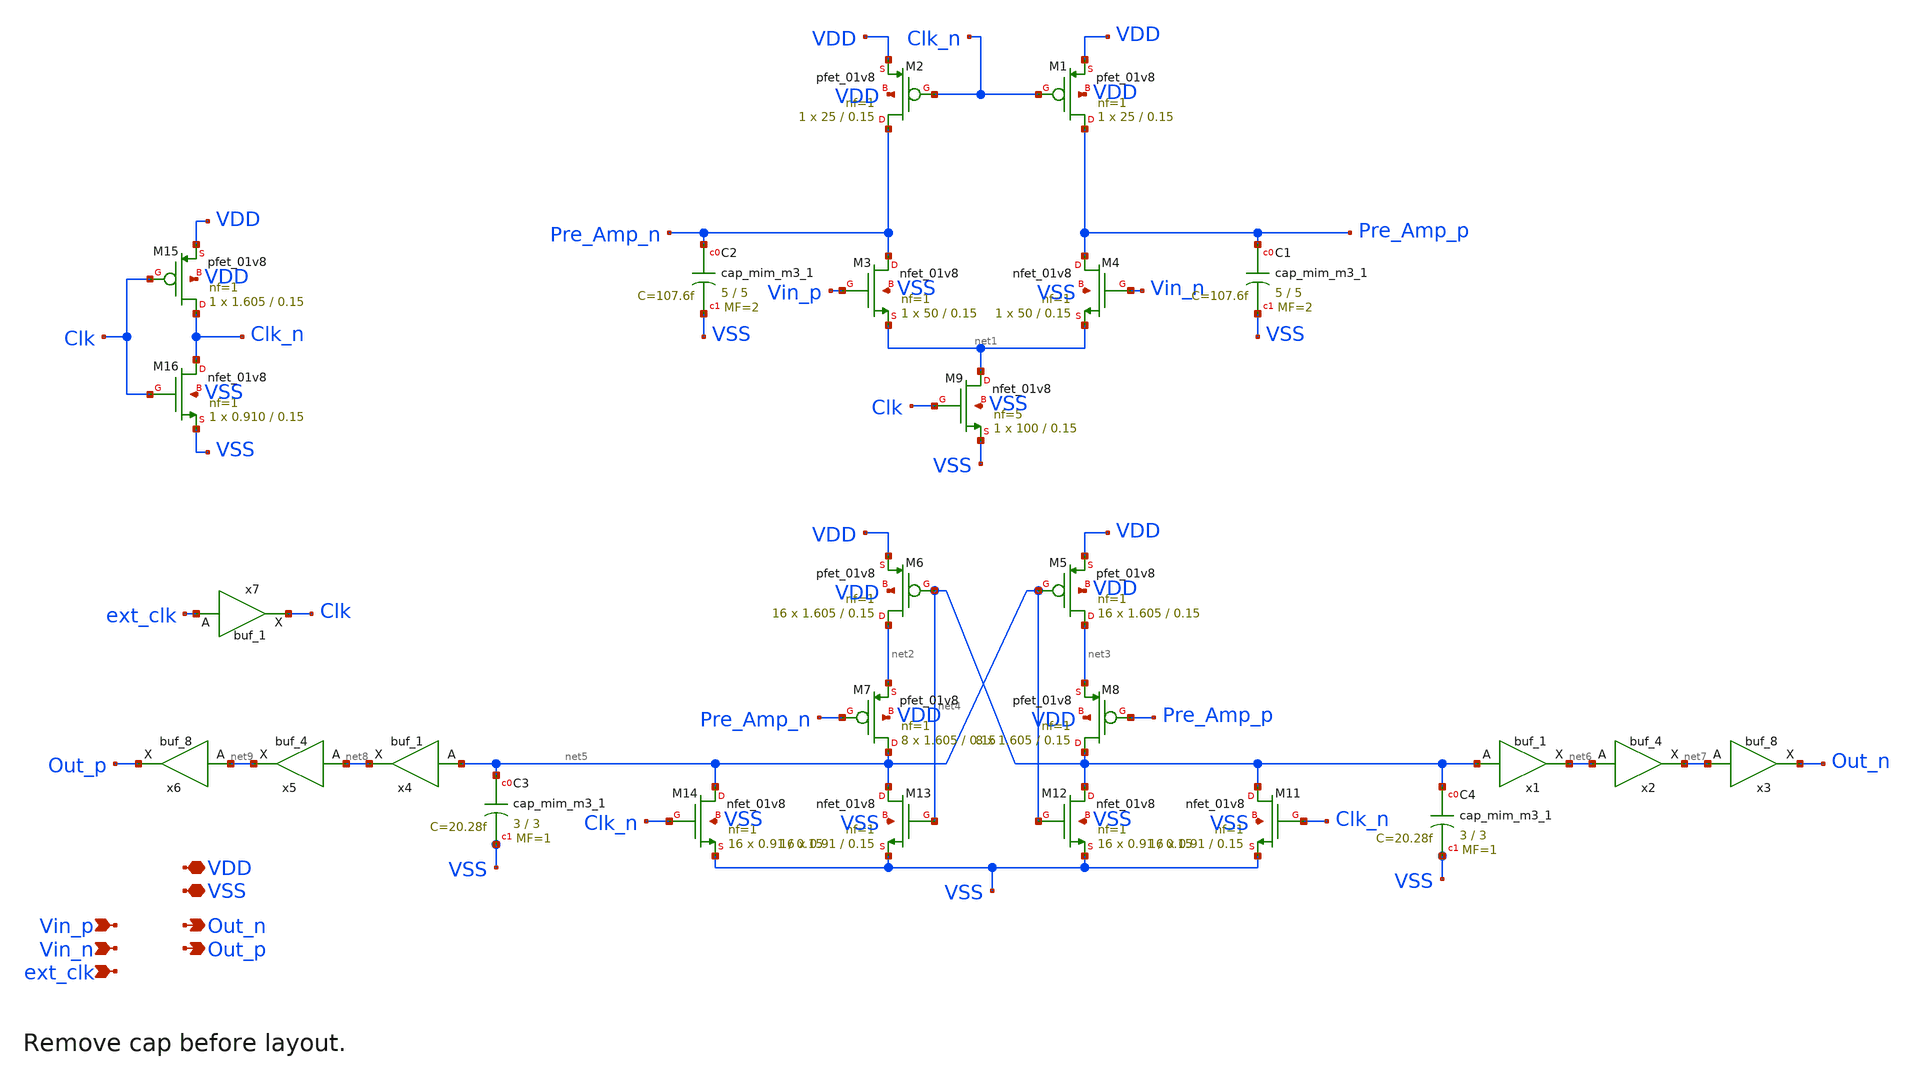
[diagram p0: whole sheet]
** sch_path: xschem/src/comparator/comparator.sch
**.subckt comparator VDD VSS Vin_p Out_n Vin_n Out_p ext_clk
*.iopin VDD
*.iopin VSS
*.ipin Vin_p
*.opin Out_n
*.ipin Vin_n
*.opin Out_p
*.ipin ext_clk
XM1 Pre_Amp_p Clk_n VDD VDD sky130_fd_pr__pfet_01v8 L=0.15 W=25 nf=1 ad='int((nf+1)/2) * W/nf * 0.29'
+ as='int((nf+2)/2) * W/nf * 0.29' pd='2*int((nf+1)/2) * (W/nf + 0.29)' ps='2*int((nf+2)/2) * (W/nf + 0.29)'
+ nrd='0.29 / W' nrs='0.29 / W' sa=0 sb=0 sd=0 mult=1 m=1
XM2 Pre_Amp_n Clk_n VDD VDD sky130_fd_pr__pfet_01v8 L=0.15 W=25 nf=1 ad='int((nf+1)/2) * W/nf * 0.29'
+ as='int((nf+2)/2) * W/nf * 0.29' pd='2*int((nf+1)/2) * (W/nf + 0.29)' ps='2*int((nf+2)/2) * (W/nf + 0.29)'
+ nrd='0.29 / W' nrs='0.29 / W' sa=0 sb=0 sd=0 mult=1 m=1
XM3 Pre_Amp_n Vin_p net1 VSS sky130_fd_pr__nfet_01v8 L=0.15 W=50 nf=1 ad='int((nf+1)/2) * W/nf * 0.29'
+ as='int((nf+2)/2) * W/nf * 0.29' pd='2*int((nf+1)/2) * (W/nf + 0.29)' ps='2*int((nf+2)/2) * (W/nf + 0.29)'
+ nrd='0.29 / W' nrs='0.29 / W' sa=0 sb=0 sd=0 mult=1 m=1
XM4 Pre_Amp_p Vin_n net1 VSS sky130_fd_pr__nfet_01v8 L=0.15 W=50 nf=1 ad='int((nf+1)/2) * W/nf * 0.29'
+ as='int((nf+2)/2) * W/nf * 0.29' pd='2*int((nf+1)/2) * (W/nf + 0.29)' ps='2*int((nf+2)/2) * (W/nf + 0.29)'
+ nrd='0.29 / W' nrs='0.29 / W' sa=0 sb=0 sd=0 mult=1 m=1
XM5 net3 net5 VDD VDD sky130_fd_pr__pfet_01v8 L=0.15 W=1.605 nf=1 ad='int((nf+1)/2) * W/nf * 0.29' as='int((nf+2)/2) * W/nf * 0.29'
+ pd='2*int((nf+1)/2) * (W/nf + 0.29)' ps='2*int((nf+2)/2) * (W/nf + 0.29)' nrd='0.29 / W' nrs='0.29 / W'
+ sa=0 sb=0 sd=0 mult=16 m=16
XM6 net2 net4 VDD VDD sky130_fd_pr__pfet_01v8 L=0.15 W=1.605 nf=1 ad='int((nf+1)/2) * W/nf * 0.29' as='int((nf+2)/2) * W/nf * 0.29'
+ pd='2*int((nf+1)/2) * (W/nf + 0.29)' ps='2*int((nf+2)/2) * (W/nf + 0.29)' nrd='0.29 / W' nrs='0.29 / W'
+ sa=0 sb=0 sd=0 mult=16 m=16
XM9 net1 Clk VSS VSS sky130_fd_pr__nfet_01v8 L=0.15 W=100 nf=5 ad='int((nf+1)/2) * W/nf * 0.29' as='int((nf+2)/2) * W/nf * 0.29'
+ pd='2*int((nf+1)/2) * (W/nf + 0.29)' ps='2*int((nf+2)/2) * (W/nf + 0.29)' nrd='0.29 / W' nrs='0.29 / W'
+ sa=0 sb=0 sd=0 mult=1 m=1
XM11 net4 Clk_n VSS VSS sky130_fd_pr__nfet_01v8 L=0.15 W=0.91 nf=1 ad='int((nf+1)/2) * W/nf * 0.29' as='int((nf+2)/2) * W/nf * 0.29'
+ pd='2*int((nf+1)/2) * (W/nf + 0.29)' ps='2*int((nf+2)/2) * (W/nf + 0.29)' nrd='0.29 / W' nrs='0.29 / W'
+ sa=0 sb=0 sd=0 mult=16 m=16
XM12 net4 net5 VSS VSS sky130_fd_pr__nfet_01v8 L=0.15 W=0.91 nf=1 ad='int((nf+1)/2) * W/nf * 0.29' as='int((nf+2)/2) * W/nf * 0.29'
+ pd='2*int((nf+1)/2) * (W/nf + 0.29)' ps='2*int((nf+2)/2) * (W/nf + 0.29)' nrd='0.29 / W' nrs='0.29 / W'
+ sa=0 sb=0 sd=0 mult=16 m=16
XM13 net5 net4 VSS VSS sky130_fd_pr__nfet_01v8 L=0.15 W=0.91 nf=1 ad='int((nf+1)/2) * W/nf * 0.29' as='int((nf+2)/2) * W/nf * 0.29'
+ pd='2*int((nf+1)/2) * (W/nf + 0.29)' ps='2*int((nf+2)/2) * (W/nf + 0.29)' nrd='0.29 / W' nrs='0.29 / W'
+ sa=0 sb=0 sd=0 mult=16 m=16
XM14 net5 Clk_n VSS VSS sky130_fd_pr__nfet_01v8 L=0.15 W=0.91 nf=1 ad='int((nf+1)/2) * W/nf * 0.29' as='int((nf+2)/2) * W/nf * 0.29'
+ pd='2*int((nf+1)/2) * (W/nf + 0.29)' ps='2*int((nf+2)/2) * (W/nf + 0.29)' nrd='0.29 / W' nrs='0.29 / W'
+ sa=0 sb=0 sd=0 mult=16 m=16
XM15 Clk_n Clk VDD VDD sky130_fd_pr__pfet_01v8 L=0.15 W=1.605 nf=1 ad='int((nf+1)/2) * W/nf * 0.29' as='int((nf+2)/2) * W/nf * 0.29'
+ pd='2*int((nf+1)/2) * (W/nf + 0.29)' ps='2*int((nf+2)/2) * (W/nf + 0.29)' nrd='0.29 / W' nrs='0.29 / W'
+ sa=0 sb=0 sd=0 mult=1 m=1
XM16 Clk_n Clk VSS VSS sky130_fd_pr__nfet_01v8 L=0.15 W=0.910 nf=1 ad='int((nf+1)/2) * W/nf * 0.29' as='int((nf+2)/2) * W/nf * 0.29'
+ pd='2*int((nf+1)/2) * (W/nf + 0.29)' ps='2*int((nf+2)/2) * (W/nf + 0.29)' nrd='0.29 / W' nrs='0.29 / W'
+ sa=0 sb=0 sd=0 mult=1 m=1
XM7 net5 Pre_Amp_n net2 VDD sky130_fd_pr__pfet_01v8 L=0.15 W=1.605 nf=1 ad='int((nf+1)/2) * W/nf * 0.29'
+ as='int((nf+2)/2) * W/nf * 0.29' pd='2*int((nf+1)/2) * (W/nf + 0.29)' ps='2*int((nf+2)/2) * (W/nf + 0.29)'
+ nrd='0.29 / W' nrs='0.29 / W' sa=0 sb=0 sd=0 mult=8 m=8
XM8 net4 Pre_Amp_p net3 VDD sky130_fd_pr__pfet_01v8 L=0.15 W=1.605 nf=1 ad='int((nf+1)/2) * W/nf * 0.29'
+ as='int((nf+2)/2) * W/nf * 0.29' pd='2*int((nf+1)/2) * (W/nf + 0.29)' ps='2*int((nf+2)/2) * (W/nf + 0.29)'
+ nrd='0.29 / W' nrs='0.29 / W' sa=0 sb=0 sd=0 mult=8 m=8
XC1 Pre_Amp_p VSS sky130_fd_pr__cap_mim_m3_1 W=5 L=5 MF=2 m=2
XC2 Pre_Amp_n VSS sky130_fd_pr__cap_mim_m3_1 W=5 L=5 MF=2 m=2
x1 net4 VSS VSS VDD VDD net6 sky130_fd_sc_hd__buf_1
x2 net6 VSS VSS VDD VDD net7 sky130_fd_sc_hd__buf_4
x3 net7 VSS VSS VDD VDD Out_n sky130_fd_sc_hd__buf_8
x4 net5 VSS VSS VDD VDD net8 sky130_fd_sc_hd__buf_1
x5 net8 VSS VSS VDD VDD net9 sky130_fd_sc_hd__buf_4
x6 net9 VSS VSS VDD VDD Out_p sky130_fd_sc_hd__buf_8
XC3 net5 VSS sky130_fd_pr__cap_mim_m3_1 W=3 L=3 MF=1 m=1
XC4 net4 VSS sky130_fd_pr__cap_mim_m3_1 W=3 L=3 MF=1 m=1
x7 ext_clk VSS VSS VDD VDD Clk sky130_fd_sc_hd__buf_1
**.ends
.end
